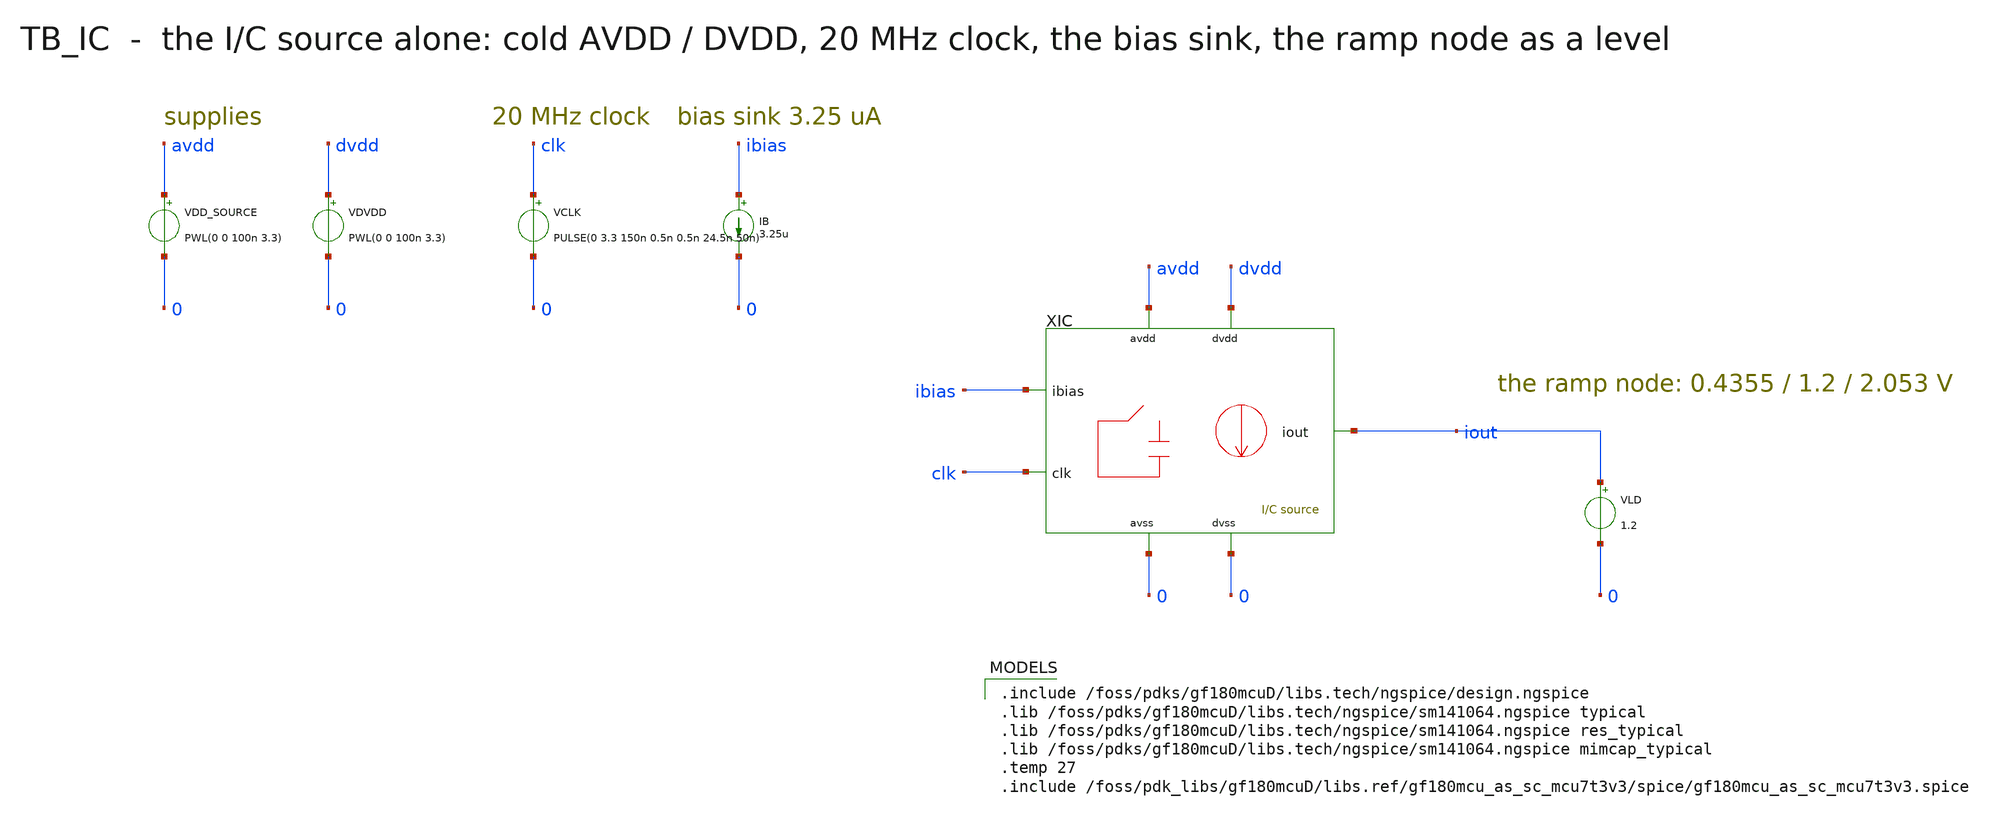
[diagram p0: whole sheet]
** sch_path: mixed_signal/ic_source/tb_ic.sch
**.subckt tb_ic
VDD_SOURCE avdd 0 PWL(0 0 100n 3.3)
VDVDD dvdd 0 PWL(0 0 100n 3.3)
VCLK clk 0 PULSE(0 3.3 150n 0.5n 0.5n 24.5n 50n)
IB ibias 0 3.25u
XIC iout ibias clk avdd dvdd 0 0 ic_source
VLD iout 0 1.2
**** begin user architecture code

.include /foss/pdks/gf180mcuD/libs.tech/ngspice/design.ngspice
.lib /foss/pdks/gf180mcuD/libs.tech/ngspice/sm141064.ngspice typical
.lib /foss/pdks/gf180mcuD/libs.tech/ngspice/sm141064.ngspice res_typical
.lib /foss/pdks/gf180mcuD/libs.tech/ngspice/sm141064.ngspice mimcap_typical
.temp 27
.include /foss/pdk_libs/gf180mcuD/libs.ref/gf180mcu_as_sc_mcu7t3v3/spice/gf180mcu_as_sc_mcu7t3v3.spice

**** end user architecture code
**.ends
.end
